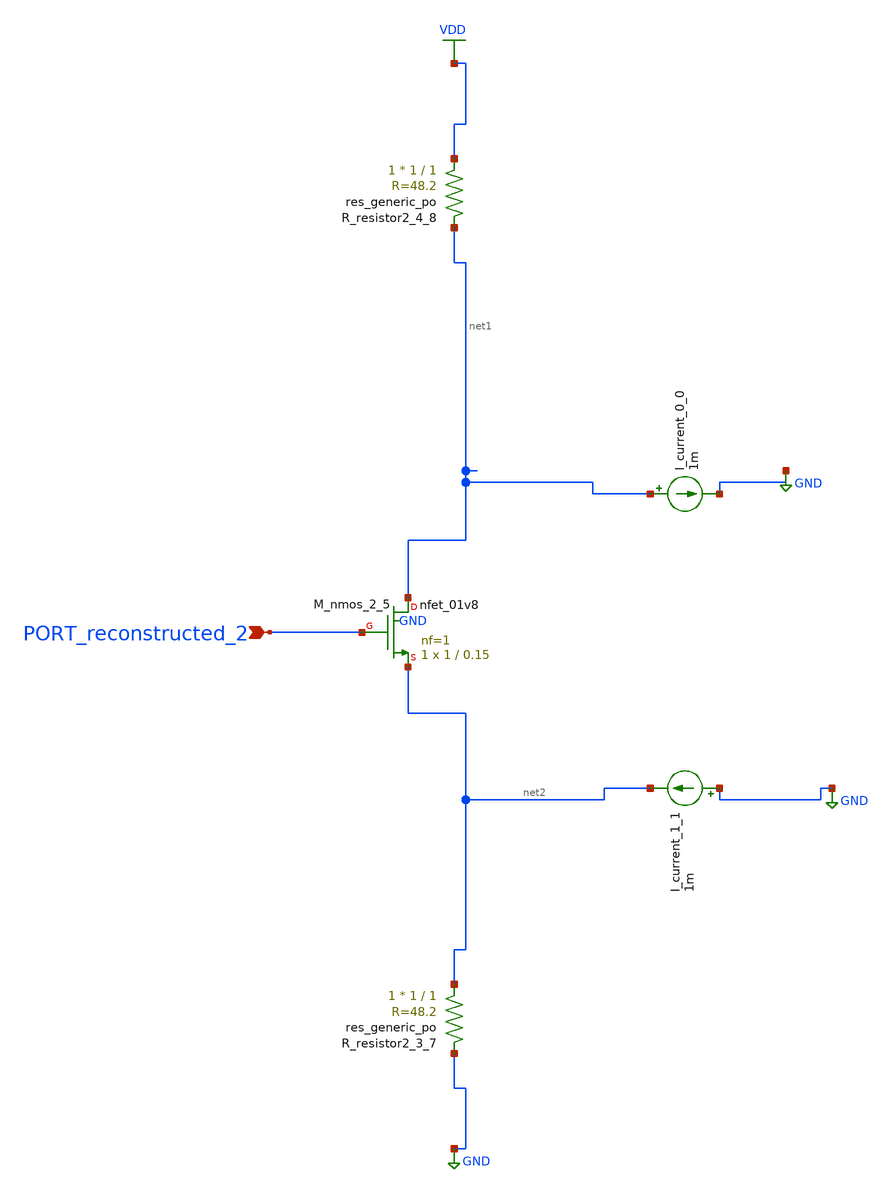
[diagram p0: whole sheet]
** sch_path: schematics/AMSNet/484.sch
**.subckt 484 PORT_reconstructed_2
*.ipin PORT_reconstructed_2
I_current_0_0 net1 GND 1m
I_current_1_1 GND net2 1m
XM_nmos_2_5 net1 PORT_reconstructed_2 net2 GND sky130_fd_pr__nfet_01v8 L=0.15 W=1 nf=1 ad='int((1 + 1)/2) * 1 / 1 * 0.29'
+ as='int((1 + 2)/2) * 1 / 1 * 0.29' pd='2*int((1 + 1)/2) * (1 / 1 + 0.29)' ps='2*int((1 + 2)/2) * (1 / 1 + 0.29)'
+ nrd='0.29 / 1 ' nrs='0.29 / 1 ' sa=0 sb=0 sd=0 mult=1 m=1
XR_resistor2_3_7 net2 GND sky130_fd_pr__res_generic_po W=1 L=1 m=1
XR_resistor2_4_8 VDD net1 sky130_fd_pr__res_generic_po W=1 L=1 m=1
**.ends
.GLOBAL GND
.GLOBAL VDD
.end
